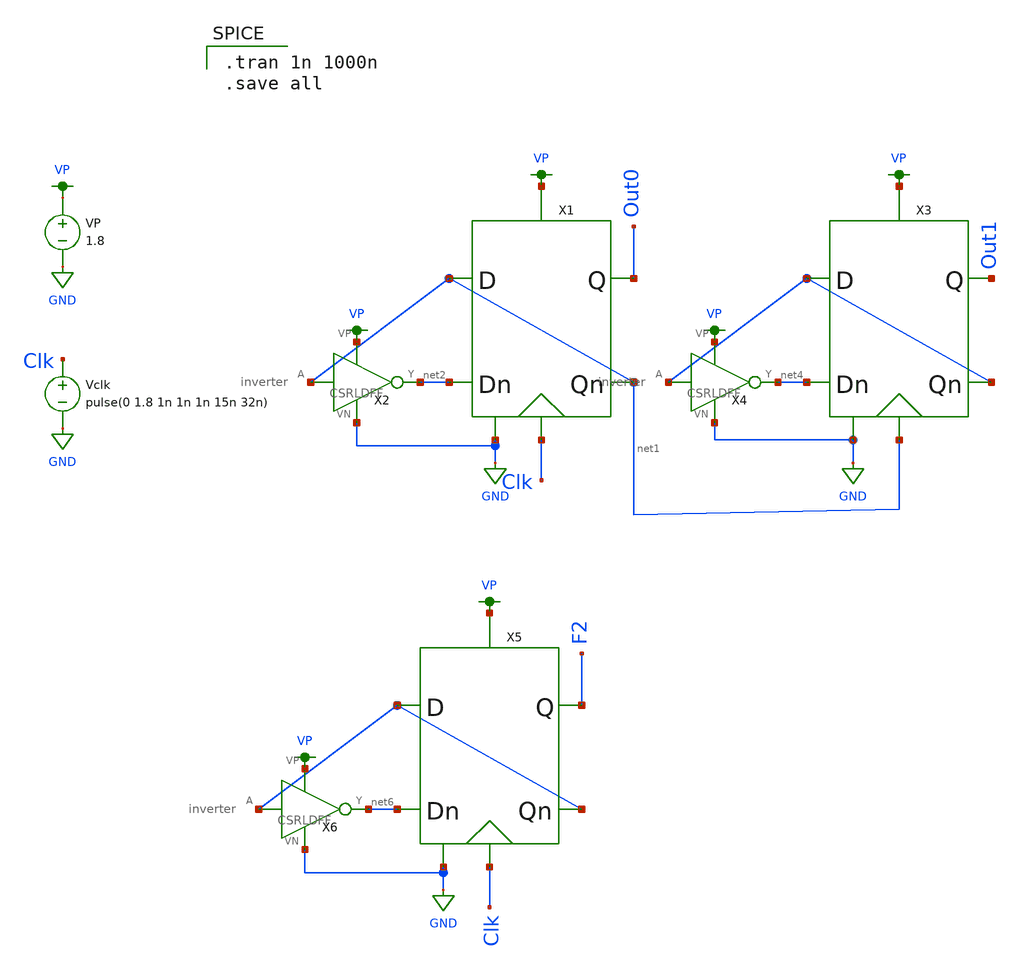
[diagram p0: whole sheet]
** sch_path: DRAM_Components/Schematic/DRAMSetup.sch
**.subckt DRAMSetup
VP VP GND 1.8
Vclk Clk GND pulse(0 1.8 1n 1n 1n 15n 32n)
X1 net1 Clk GND VP net1 Out0 net2 CSRLDFF
X2 net1 net2 VP GND inverter
X3 net3 net1 GND VP net3 Out1 net4 CSRLDFF
X4 net3 net4 VP GND inverter
X5 net5 Clk GND VP net5 F2 net6 CSRLDFF
X6 net5 net6 VP GND inverter
**** begin user architecture code

.option wnflag=1
.param MC_SWITCH=0.0
.lib ~/skywater/skywater-pdk/libraries/sky130_fd_pr_ngspice/latest/models/sky130.lib.spice tt


.tran 1n 1000n
.save all

**** end user architecture code
**.ends

* expanding   symbol:  /home/madvlsi/Desktop/CMOSDRAM/DRAM_Components/Schematic/CSRLDFF.sym # of
*+ pins=7
** sym_path: DRAM_Components/Schematic/CSRLDFF.sym
** sch_path: DRAM_Components/Schematic/CSRLDFF.sch
.subckt CSRLDFF D clk VN VP Qn Q Dn
*.ipin D
*.ipin clk
*.iopin VN
*.opin Q
*.opin Qn
*.ipin Dn
*.iopin VP
XM1 net3 clk D VP sky130_fd_pr__pfet_01v8 L=0.6 W=1 nf=1 ad='int((nf+1)/2) * W/nf * 0.29' as='int((nf+2)/2) * W/nf * 0.29'
+ pd='2*int((nf+1)/2) * (W/nf + 0.29)' ps='2*int((nf+2)/2) * (W/nf + 0.29)' nrd='0.29 / W' nrs='0.29 / W'
+ sa=0 sb=0 sd=0 mult=1 m=1
XM2 net2 clk Dn VP sky130_fd_pr__pfet_01v8 L=0.6 W=1 nf=1 ad='int((nf+1)/2) * W/nf * 0.29' as='int((nf+2)/2) * W/nf * 0.29'
+ pd='2*int((nf+1)/2) * (W/nf + 0.29)' ps='2*int((nf+2)/2) * (W/nf + 0.29)' nrd='0.29 / W' nrs='0.29 / W'
+ sa=0 sb=0 sd=0 mult=1 m=1
XM3 net3 clk Q VN sky130_fd_pr__nfet_01v8 L=0.6 W=1 nf=1 ad='int((nf+1)/2) * W/nf * 0.29' as='int((nf+2)/2) * W/nf * 0.29'
+ pd='2*int((nf+1)/2) * (W/nf + 0.29)' ps='2*int((nf+2)/2) * (W/nf + 0.29)' nrd='0.29 / W' nrs='0.29 / W'
+ sa=0 sb=0 sd=0 mult=1 m=1
XM4 net2 clk Qn VN sky130_fd_pr__nfet_01v8 L=0.6 W=1 nf=1 ad='int((nf+1)/2) * W/nf * 0.29' as='int((nf+2)/2) * W/nf * 0.29'
+ pd='2*int((nf+1)/2) * (W/nf + 0.29)' ps='2*int((nf+2)/2) * (W/nf + 0.29)' nrd='0.29 / W' nrs='0.29 / W'
+ sa=0 sb=0 sd=0 mult=1 m=1
XM5 net1 clk VN VN sky130_fd_pr__nfet_01v8 L=0.15 W=1 nf=1 ad='int((nf+1)/2) * W/nf * 0.29' as='int((nf+2)/2) * W/nf * 0.29'
+ pd='2*int((nf+1)/2) * (W/nf + 0.29)' ps='2*int((nf+2)/2) * (W/nf + 0.29)' nrd='0.29 / W' nrs='0.29 / W'
+ sa=0 sb=0 sd=0 mult=1 m=1
XM6 net2 net3 net1 VN sky130_fd_pr__nfet_01v8 L=0.15 W=1 nf=1 ad='int((nf+1)/2) * W/nf * 0.29' as='int((nf+2)/2) * W/nf * 0.29'
+ pd='2*int((nf+1)/2) * (W/nf + 0.29)' ps='2*int((nf+2)/2) * (W/nf + 0.29)' nrd='0.29 / W' nrs='0.29 / W'
+ sa=0 sb=0 sd=0 mult=1 m=1
XM7 net3 net2 net1 VN sky130_fd_pr__nfet_01v8 L=0.15 W=1 nf=1 ad='int((nf+1)/2) * W/nf * 0.29' as='int((nf+2)/2) * W/nf * 0.29'
+ pd='2*int((nf+1)/2) * (W/nf + 0.29)' ps='2*int((nf+2)/2) * (W/nf + 0.29)' nrd='0.29 / W' nrs='0.29 / W'
+ sa=0 sb=0 sd=0 mult=1 m=1
XM8 net2 net3 VP VP sky130_fd_pr__pfet_01v8 L=0.15 W=1 nf=1 ad='int((nf+1)/2) * W/nf * 0.29' as='int((nf+2)/2) * W/nf * 0.29'
+ pd='2*int((nf+1)/2) * (W/nf + 0.29)' ps='2*int((nf+2)/2) * (W/nf + 0.29)' nrd='0.29 / W' nrs='0.29 / W'
+ sa=0 sb=0 sd=0 mult=1 m=1
XM9 net3 net2 VP VP sky130_fd_pr__pfet_01v8 L=0.15 W=1 nf=1 ad='int((nf+1)/2) * W/nf * 0.29' as='int((nf+2)/2) * W/nf * 0.29'
+ pd='2*int((nf+1)/2) * (W/nf + 0.29)' ps='2*int((nf+2)/2) * (W/nf + 0.29)' nrd='0.29 / W' nrs='0.29 / W'
+ sa=0 sb=0 sd=0 mult=1 m=1
XM10 net4 clk VP VP sky130_fd_pr__pfet_01v8 L=0.15 W=1 nf=1 ad='int((nf+1)/2) * W/nf * 0.29' as='int((nf+2)/2) * W/nf * 0.29'
+ pd='2*int((nf+1)/2) * (W/nf + 0.29)' ps='2*int((nf+2)/2) * (W/nf + 0.29)' nrd='0.29 / W' nrs='0.29 / W'
+ sa=0 sb=0 sd=0 mult=1 m=1
XM11 Qn Q net4 VP sky130_fd_pr__pfet_01v8 L=0.15 W=1 nf=1 ad='int((nf+1)/2) * W/nf * 0.29' as='int((nf+2)/2) * W/nf * 0.29'
+ pd='2*int((nf+1)/2) * (W/nf + 0.29)' ps='2*int((nf+2)/2) * (W/nf + 0.29)' nrd='0.29 / W' nrs='0.29 / W'
+ sa=0 sb=0 sd=0 mult=1 m=1
XM12 Q Qn net4 VP sky130_fd_pr__pfet_01v8 L=0.15 W=1 nf=1 ad='int((nf+1)/2) * W/nf * 0.29' as='int((nf+2)/2) * W/nf * 0.29'
+ pd='2*int((nf+1)/2) * (W/nf + 0.29)' ps='2*int((nf+2)/2) * (W/nf + 0.29)' nrd='0.29 / W' nrs='0.29 / W'
+ sa=0 sb=0 sd=0 mult=1 m=1
XM13 Qn Q VN VN sky130_fd_pr__nfet_01v8 L=0.15 W=1 nf=1 ad='int((nf+1)/2) * W/nf * 0.29' as='int((nf+2)/2) * W/nf * 0.29'
+ pd='2*int((nf+1)/2) * (W/nf + 0.29)' ps='2*int((nf+2)/2) * (W/nf + 0.29)' nrd='0.29 / W' nrs='0.29 / W'
+ sa=0 sb=0 sd=0 mult=1 m=1
XM14 Q Qn VN VN sky130_fd_pr__nfet_01v8 L=0.15 W=1 nf=1 ad='int((nf+1)/2) * W/nf * 0.29' as='int((nf+2)/2) * W/nf * 0.29'
+ pd='2*int((nf+1)/2) * (W/nf + 0.29)' ps='2*int((nf+2)/2) * (W/nf + 0.29)' nrd='0.29 / W' nrs='0.29 / W'
+ sa=0 sb=0 sd=0 mult=1 m=1
.ends


* expanding   symbol:  /home/madvlsi/Desktop/CMOSDRAM/DRAM_Components/Schematic/inverter.sym # of
*+ pins=4
** sym_path: DRAM_Components/Schematic/inverter.sym
** sch_path: DRAM_Components/Schematic/inverter.sch
.subckt inverter A Y VP VN
*.ipin A
*.iopin VP
*.opin Y
*.iopin VN
XM1 Y A VP VP sky130_fd_pr__pfet_01v8 L=0.15 W=1 nf=1 ad='int((nf+1)/2) * W/nf * 0.29' as='int((nf+2)/2) * W/nf * 0.29'
+ pd='2*int((nf+1)/2) * (W/nf + 0.29)' ps='2*int((nf+2)/2) * (W/nf + 0.29)' nrd='0.29 / W' nrs='0.29 / W'
+ sa=0 sb=0 sd=0 mult=1 m=1
XM2 Y A VN VN sky130_fd_pr__nfet_01v8 L=0.15 W=1 nf=1 ad='int((nf+1)/2) * W/nf * 0.29' as='int((nf+2)/2) * W/nf * 0.29'
+ pd='2*int((nf+1)/2) * (W/nf + 0.29)' ps='2*int((nf+2)/2) * (W/nf + 0.29)' nrd='0.29 / W' nrs='0.29 / W'
+ sa=0 sb=0 sd=0 mult=1 m=1
.ends

.GLOBAL GND
.GLOBAL VP
.end
